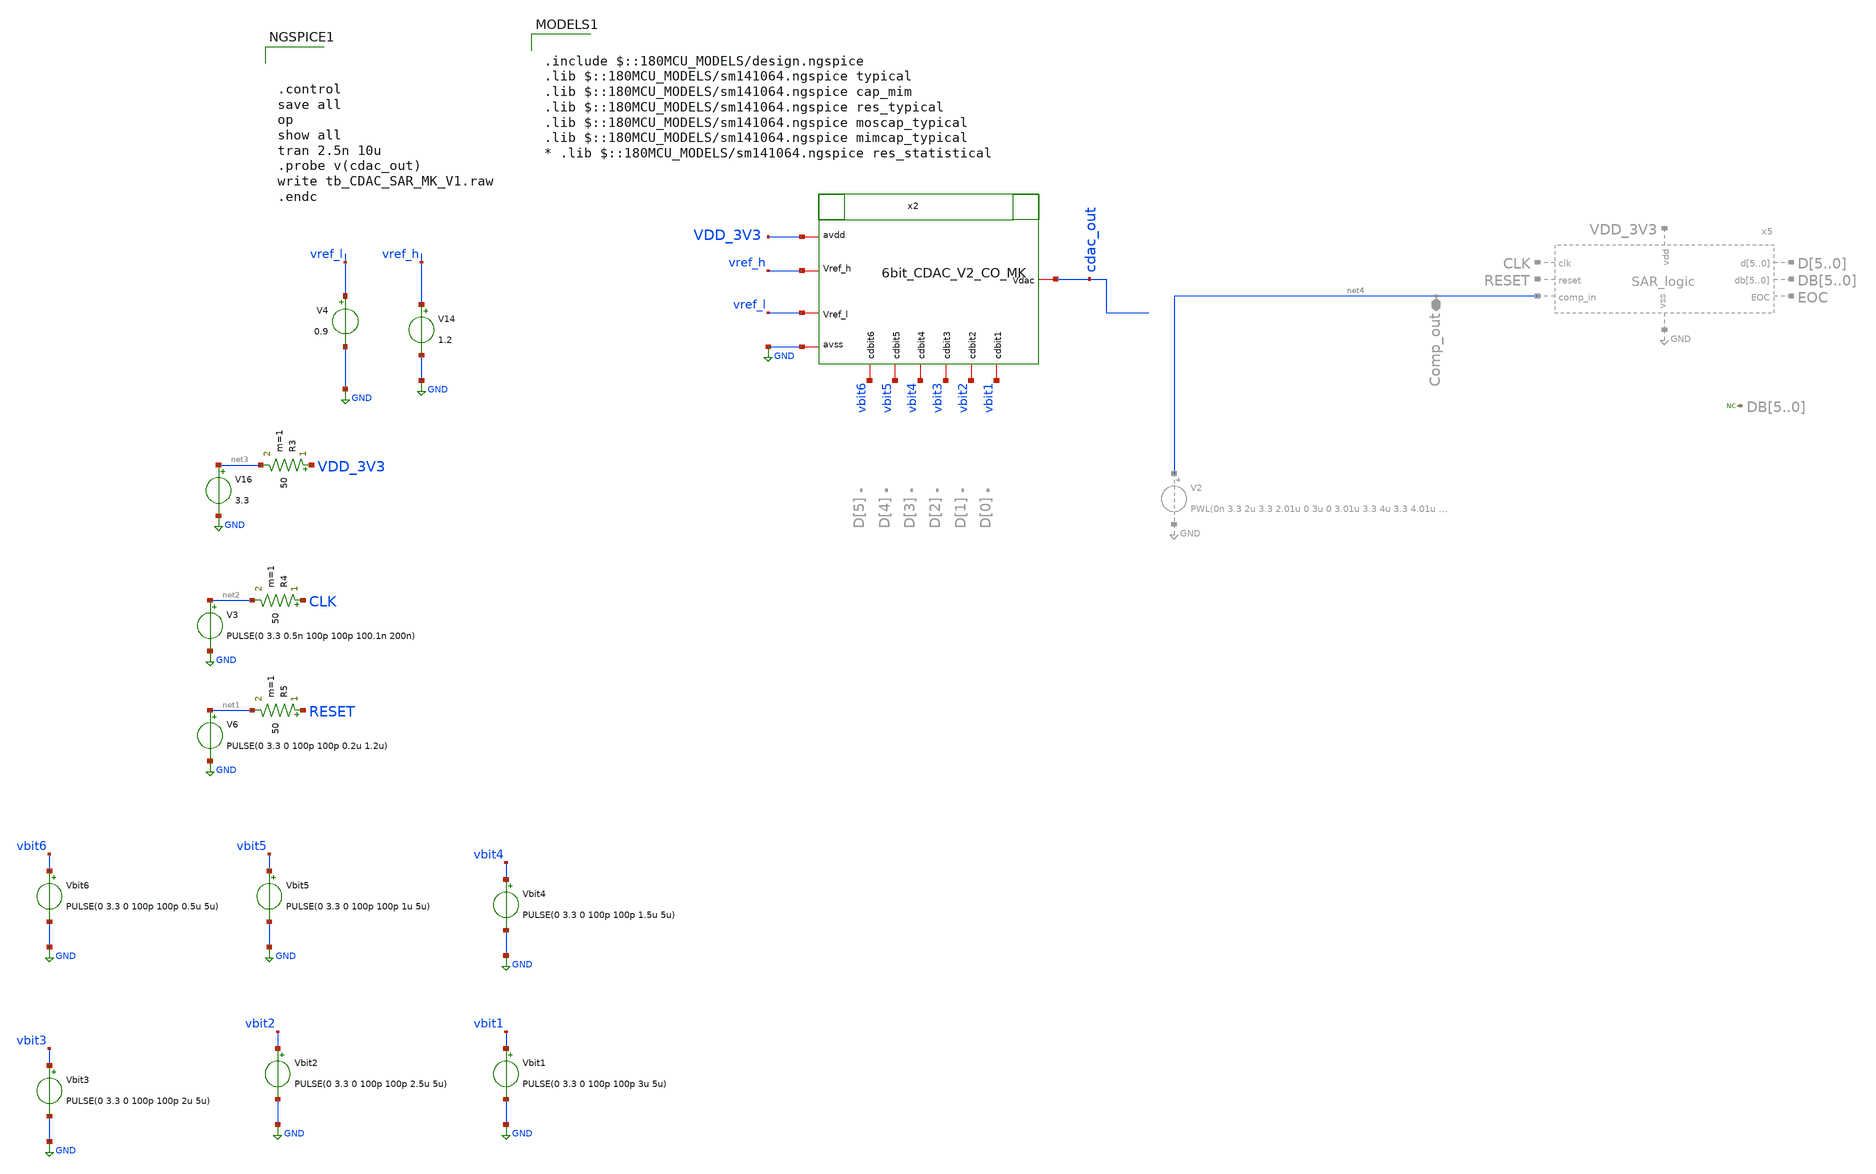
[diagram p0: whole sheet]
** sch_path: designs/full_ADC/TB_CDAC_SAR_MK_V1.sch
**.subckt TB_CDAC_SAR_MK_V1
V14 vref_h GND 1.2
V6 net1 GND PULSE(0 3.3 0 100p 100p 0.2u 1.2u)
R5 RESET net1 50 m=1
V3 net2 GND PULSE(0 3.3 0.5n 100p 100p 100.1n 200n)
R4 CLK net2 50 m=1
x2 vref_l cdac_out VDD_3V3 GND vref_h vbit6 vbit5 vbit3 vbit1 vbit2 vbit4 6bit_CDAC_V2_CO_MK
V4 vref_l GND 0.9
V16 net3 GND 3.3
R3 VDD_3V3 net3 50 m=1
Vbit1 vbit1 GND PULSE(0 3.3 0 100p 100p 3u 5u)
Vbit2 vbit2 GND PULSE(0 3.3 0 100p 100p 2.5u 5u)
Vbit3 vbit3 GND PULSE(0 3.3 0 100p 100p 2u 5u)
Vbit4 vbit4 GND PULSE(0 3.3 0 100p 100p 1.5u 5u)
Vbit5 vbit5 GND PULSE(0 3.3 0 100p 100p 1u 5u)
Vbit6 vbit6 GND PULSE(0 3.3 0 100p 100p 0.5u 5u)
**** begin user architecture code



.control
save all
op
show all
tran 2.5n 10u
.probe v(cdac_out)
write tb_CDAC_SAR_MK_V1.raw
.endc



.include $::180MCU_MODELS/design.ngspice
.lib $::180MCU_MODELS/sm141064.ngspice typical
.lib $::180MCU_MODELS/sm141064.ngspice cap_mim
.lib $::180MCU_MODELS/sm141064.ngspice res_typical
.lib $::180MCU_MODELS/sm141064.ngspice moscap_typical
.lib $::180MCU_MODELS/sm141064.ngspice mimcap_typical
* .lib $::180MCU_MODELS/sm141064.ngspice res_statistical

**** end user architecture code
**.ends
.GLOBAL GND
.end
